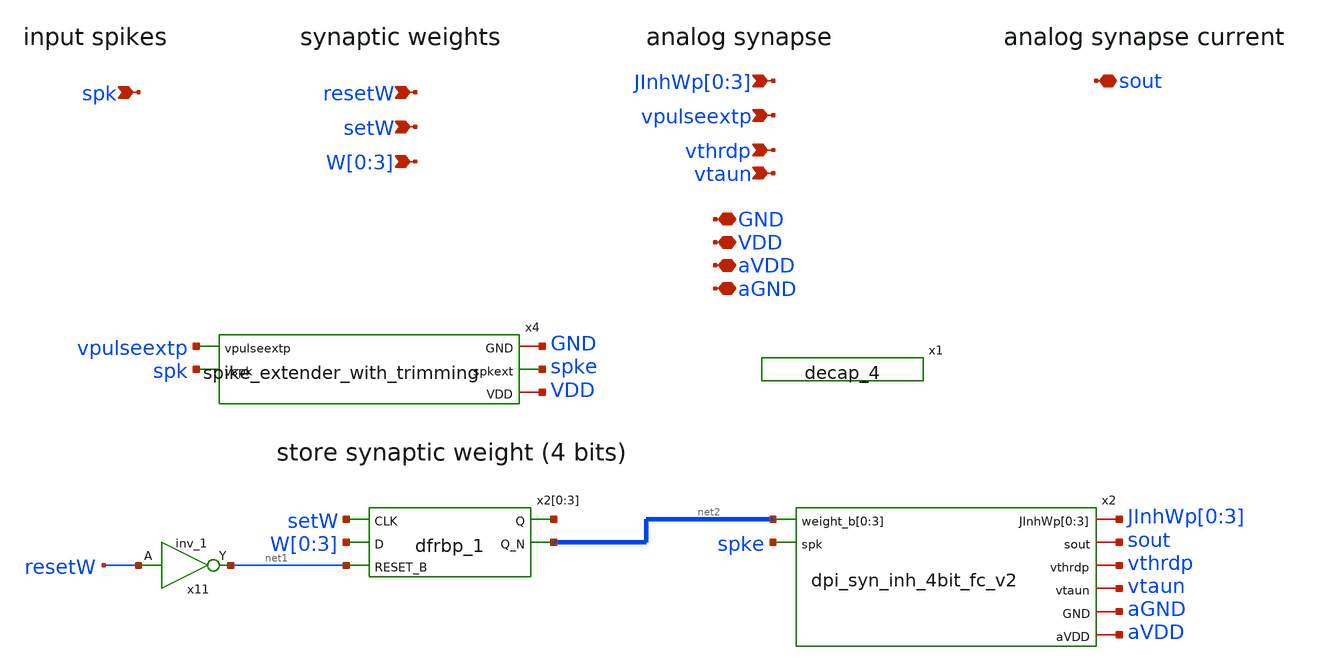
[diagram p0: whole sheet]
** sch_path: design/xschem/synapse_4bit_memory_inh_v1_norail.sch
**.subckt synapse_4bit_memory_inh_v1_norail vpulseextp spk JInhWp[0],JInhWp[1],JInhWp[2],JInhWp[3]
*+ W[0],W[1],W[2],W[3] setW resetW sout vthrdp vtaun GND VDD aVDD aGND
*.ipin vpulseextp
*.ipin spk
*.ipin JInhWp[0],JInhWp[1],JInhWp[2],JInhWp[3]
*.ipin W[0],W[1],W[2],W[3]
*.ipin setW
*.ipin resetW
*.iopin sout
*.ipin vthrdp
*.ipin vtaun
*.iopin GND
*.iopin VDD
*.iopin aVDD
*.iopin aGND
x11 resetW GND GND VDD VDD net1 sky130_fd_sc_hd__inv_1
x2 JInhWp[0] JInhWp[1] JInhWp[2] JInhWp[3] net2[3] net2[2] net2[1] net2[0] spke sout vthrdp vtaun
+ aGND aVDD dpi_syn_inh_4bit_fc_v2
x2[0] setW W[0] net1 GND GND VDD VDD net3[3] net2[3] sky130_fd_sc_hd__dfrbp_1
x2[1] setW W[1] net1 GND GND VDD VDD net3[2] net2[2] sky130_fd_sc_hd__dfrbp_1
x2[2] setW W[2] net1 GND GND VDD VDD net3[1] net2[1] sky130_fd_sc_hd__dfrbp_1
x2[3] setW W[3] net1 GND GND VDD VDD net3[0] net2[0] sky130_fd_sc_hd__dfrbp_1
x4 vpulseextp spk GND spke VDD spike_extender_with_trimming
x1 GND GND VDD VDD sky130_fd_sc_hd__decap_4
**.ends

* expanding   symbol:  dpi_syn_inh_4bit_fc_v2.sym # of pins=8
** sym_path: design/xschem/dpi_syn_inh_4bit_fc_v2.sym
** sch_path: design/xschem/dpi_syn_inh_4bit_fc_v2.sch
.subckt dpi_syn_inh_4bit_fc_v2 JInhWp[0] JInhWp[1] JInhWp[2] JInhWp[3] weight_b[0] weight_b[1]
+ weight_b[2] weight_b[3] spk sout vthrdp vtaun GND aVDD
*.ipin spk
*.iopin vthrdp
*.iopin vtaun
*.iopin sout
*.iopin GND
*.iopin aVDD
*.ipin weight_b[0],weight_b[1],weight_b[2],weight_b[3]
*.iopin JInhWp[0],JInhWp[1],JInhWp[2],JInhWp[3]
XM5 net2 net3 net1 aVDD sky130_fd_pr__pfet_01v8 L=0.2 W=1.2 nf=1 ad='int((nf+1)/2) * W/nf * 0.29' as='int((nf+2)/2) * W/nf * 0.29'
+ pd='2*int((nf+1)/2) * (W/nf + 0.29)' ps='2*int((nf+2)/2) * (W/nf + 0.29)' nrd='0.29 / W' nrs='0.29 / W'
+ sa=0 sb=0 sd=0 mult=1 m=1
XM2 GND vthrdp net2 aVDD sky130_fd_pr__pfet_01v8 L=0.2 W=1.2 nf=1 ad='int((nf+1)/2) * W/nf * 0.29' as='int((nf+2)/2) * W/nf * 0.29'
+ pd='2*int((nf+1)/2) * (W/nf + 0.29)' ps='2*int((nf+2)/2) * (W/nf + 0.29)' nrd='0.29 / W' nrs='0.29 / W'
+ sa=0 sb=0 sd=0 mult=1 m=1
XM3 vsin vsin net2 aVDD sky130_fd_pr__pfet_01v8 L=0.2 W=1.2 nf=1 ad='int((nf+1)/2) * W/nf * 0.29' as='int((nf+2)/2) * W/nf * 0.29'
+ pd='2*int((nf+1)/2) * (W/nf + 0.29)' ps='2*int((nf+2)/2) * (W/nf + 0.29)' nrd='0.29 / W' nrs='0.29 / W'
+ sa=0 sb=0 sd=0 mult=1 m=1
XM4 vsin vtaun GND GND sky130_fd_pr__nfet_01v8 L=0.25 W=1.0 nf=1 ad='int((nf+1)/2) * W/nf * 0.29' as='int((nf+2)/2) * W/nf * 0.29'
+ pd='2*int((nf+1)/2) * (W/nf + 0.29)' ps='2*int((nf+2)/2) * (W/nf + 0.29)' nrd='0.29 / W' nrs='0.29 / W'
+ sa=0 sb=0 sd=0 mult=1 m=1
XM6 sout vsin GND GND sky130_fd_pr__nfet_01v8 L=0.25 W=1.0 nf=1 ad='int((nf+1)/2) * W/nf * 0.29' as='int((nf+2)/2) * W/nf * 0.29'
+ pd='2*int((nf+1)/2) * (W/nf + 0.29)' ps='2*int((nf+2)/2) * (W/nf + 0.29)' nrd='0.29 / W' nrs='0.29 / W'
+ sa=0 sb=0 sd=0 mult=1 m=1
XM7 net3 spk GND GND sky130_fd_pr__nfet_01v8 L=0.25 W=1.0 nf=1 ad='int((nf+1)/2) * W/nf * 0.29' as='int((nf+2)/2) * W/nf * 0.29'
+ pd='2*int((nf+1)/2) * (W/nf + 0.29)' ps='2*int((nf+2)/2) * (W/nf + 0.29)' nrd='0.29 / W' nrs='0.29 / W'
+ sa=0 sb=0 sd=0 mult=1 m=1
XM8 net3 spk aVDD aVDD sky130_fd_pr__pfet_01v8 L=0.2 W=1.2 nf=1 ad='int((nf+1)/2) * W/nf * 0.29' as='int((nf+2)/2) * W/nf * 0.29'
+ pd='2*int((nf+1)/2) * (W/nf + 0.29)' ps='2*int((nf+2)/2) * (W/nf + 0.29)' nrd='0.29 / W' nrs='0.29 / W'
+ sa=0 sb=0 sd=0 mult=1 m=1
XC1 vsin GND sky130_fd_pr__cap_mim_m3_1 W=5 L=5 MF=1 m=1
XM9 net4 JInhWp[0] aVDD aVDD sky130_fd_pr__pfet_01v8 L=1.2 W=1.2 nf=1 ad='int((nf+1)/2) * W/nf * 0.29'
+ as='int((nf+2)/2) * W/nf * 0.29' pd='2*int((nf+1)/2) * (W/nf + 0.29)' ps='2*int((nf+2)/2) * (W/nf + 0.29)'
+ nrd='0.29 / W' nrs='0.29 / W' sa=0 sb=0 sd=0 mult=1 m=1
XM10 net1 weight_b[0] net4 aVDD sky130_fd_pr__pfet_01v8 L=0.2 W=1.2 nf=1 ad='int((nf+1)/2) * W/nf * 0.29'
+ as='int((nf+2)/2) * W/nf * 0.29' pd='2*int((nf+1)/2) * (W/nf + 0.29)' ps='2*int((nf+2)/2) * (W/nf + 0.29)'
+ nrd='0.29 / W' nrs='0.29 / W' sa=0 sb=0 sd=0 mult=1 m=1
XM11 net1 weight_b[1] net5 aVDD sky130_fd_pr__pfet_01v8 L=0.2 W=1.2 nf=1 ad='int((nf+1)/2) * W/nf * 0.29'
+ as='int((nf+2)/2) * W/nf * 0.29' pd='2*int((nf+1)/2) * (W/nf + 0.29)' ps='2*int((nf+2)/2) * (W/nf + 0.29)'
+ nrd='0.29 / W' nrs='0.29 / W' sa=0 sb=0 sd=0 mult=1 m=1
XM1 net5 JInhWp[1] aVDD aVDD sky130_fd_pr__pfet_01v8 L=2.0 W=1.2 nf=1 ad='int((nf+1)/2) * W/nf * 0.29'
+ as='int((nf+2)/2) * W/nf * 0.29' pd='2*int((nf+1)/2) * (W/nf + 0.29)' ps='2*int((nf+2)/2) * (W/nf + 0.29)'
+ nrd='0.29 / W' nrs='0.29 / W' sa=0 sb=0 sd=0 mult=1 m=1
XM12 net6 JInhWp[2] aVDD aVDD sky130_fd_pr__pfet_01v8 L=4.0 W=1.2 nf=1 ad='int((nf+1)/2) * W/nf * 0.29'
+ as='int((nf+2)/2) * W/nf * 0.29' pd='2*int((nf+1)/2) * (W/nf + 0.29)' ps='2*int((nf+2)/2) * (W/nf + 0.29)'
+ nrd='0.29 / W' nrs='0.29 / W' sa=0 sb=0 sd=0 mult=1 m=1
XM13 net7 JInhWp[3] aVDD aVDD sky130_fd_pr__pfet_01v8 L=8.0 W=1.2 nf=1 ad='int((nf+1)/2) * W/nf * 0.29'
+ as='int((nf+2)/2) * W/nf * 0.29' pd='2*int((nf+1)/2) * (W/nf + 0.29)' ps='2*int((nf+2)/2) * (W/nf + 0.29)'
+ nrd='0.29 / W' nrs='0.29 / W' sa=0 sb=0 sd=0 mult=1 m=1
XM14 net1 weight_b[2] net6 aVDD sky130_fd_pr__pfet_01v8 L=0.2 W=1.2 nf=1 ad='int((nf+1)/2) * W/nf * 0.29'
+ as='int((nf+2)/2) * W/nf * 0.29' pd='2*int((nf+1)/2) * (W/nf + 0.29)' ps='2*int((nf+2)/2) * (W/nf + 0.29)'
+ nrd='0.29 / W' nrs='0.29 / W' sa=0 sb=0 sd=0 mult=1 m=1
XM15 net1 weight_b[3] net7 aVDD sky130_fd_pr__pfet_01v8 L=0.2 W=1.2 nf=1 ad='int((nf+1)/2) * W/nf * 0.29'
+ as='int((nf+2)/2) * W/nf * 0.29' pd='2*int((nf+1)/2) * (W/nf + 0.29)' ps='2*int((nf+2)/2) * (W/nf + 0.29)'
+ nrd='0.29 / W' nrs='0.29 / W' sa=0 sb=0 sd=0 mult=1 m=1
.ends


* expanding   symbol:  spike_extender_with_trimming.sym # of pins=5
** sym_path: design/xschem/spike_extender_with_trimming.sym
** sch_path: design/xschem/spike_extender_with_trimming.sch
.subckt spike_extender_with_trimming vpulseextp vspk GND spkext VDD
*.iopin GND
*.iopin VDD
*.ipin vspk
*.opin spkext
*.ipin vpulseextp
x1 vpulseextp vpulseshort GND spkext VDD spike_extender
x3 vspk GND GND VDD VDD net1 sky130_fd_sc_hd__clkdlybuf4s50_1
x2 net1 vspk GND GND VDD VDD vpulseshort sky130_fd_sc_hd__nor2b_1
.ends


* expanding   symbol:  spike_extender.sym # of pins=5
** sym_path: design/xschem/spike_extender.sym
** sch_path: design/xschem/spike_extender.sch
.subckt spike_extender vpulseextp spk GND spkext VDD
*.iopin GND
*.iopin VDD
*.ipin spk
*.opin spkext
*.ipin vpulseextp
XM1 net1 spk GND GND sky130_fd_pr__nfet_01v8 L=0.15 W=0.65 nf=1 ad='int((nf+1)/2) * W/nf * 0.29' as='int((nf+2)/2) * W/nf * 0.29'
+ pd='2*int((nf+1)/2) * (W/nf + 0.29)' ps='2*int((nf+2)/2) * (W/nf + 0.29)' nrd='0.29 / W' nrs='0.29 / W'
+ sa=0 sb=0 sd=0 mult=1 m=1
XM6 net1 vpulseextp VDD VDD sky130_fd_pr__pfet_01v8 L=2 W=1 nf=1 ad='int((nf+1)/2) * W/nf * 0.29' as='int((nf+2)/2) * W/nf * 0.29'
+ pd='2*int((nf+1)/2) * (W/nf + 0.29)' ps='2*int((nf+2)/2) * (W/nf + 0.29)' nrd='0.29 / W' nrs='0.29 / W'
+ sa=0 sb=0 sd=0 mult=1 m=1
XM5 net3 net2 GND GND sky130_fd_pr__nfet_01v8 L=0.15 W=0.65 nf=1 ad='int((nf+1)/2) * W/nf * 0.29' as='int((nf+2)/2) * W/nf * 0.29'
+ pd='2*int((nf+1)/2) * (W/nf + 0.29)' ps='2*int((nf+2)/2) * (W/nf + 0.29)' nrd='0.29 / W' nrs='0.29 / W'
+ sa=0 sb=0 sd=0 mult=1 m=1
XM8 spkext net3 GND GND sky130_fd_pr__nfet_01v8 L=0.15 W=0.65 nf=1 ad='int((nf+1)/2) * W/nf * 0.29' as='int((nf+2)/2) * W/nf * 0.29'
+ pd='2*int((nf+1)/2) * (W/nf + 0.29)' ps='2*int((nf+2)/2) * (W/nf + 0.29)' nrd='0.29 / W' nrs='0.29 / W'
+ sa=0 sb=0 sd=0 mult=1 m=1
XM4 net3 net2 VDD VDD sky130_fd_pr__pfet_01v8 L=0.15 W=1.0 nf=1 ad='int((nf+1)/2) * W/nf * 0.29' as='int((nf+2)/2) * W/nf * 0.29'
+ pd='2*int((nf+1)/2) * (W/nf + 0.29)' ps='2*int((nf+2)/2) * (W/nf + 0.29)' nrd='0.29 / W' nrs='0.29 / W'
+ sa=0 sb=0 sd=0 mult=1 m=1
XM7 spkext net3 VDD VDD sky130_fd_pr__pfet_01v8 L=0.15 W=1.0 nf=1 ad='int((nf+1)/2) * W/nf * 0.29' as='int((nf+2)/2) * W/nf * 0.29'
+ pd='2*int((nf+1)/2) * (W/nf + 0.29)' ps='2*int((nf+2)/2) * (W/nf + 0.29)' nrd='0.29 / W' nrs='0.29 / W'
+ sa=0 sb=0 sd=0 mult=1 m=1
XM2 net2 net1 GND GND sky130_fd_pr__nfet_01v8 L=0.15 W=0.65 nf=1 ad='int((nf+1)/2) * W/nf * 0.29' as='int((nf+2)/2) * W/nf * 0.29'
+ pd='2*int((nf+1)/2) * (W/nf + 0.29)' ps='2*int((nf+2)/2) * (W/nf + 0.29)' nrd='0.29 / W' nrs='0.29 / W'
+ sa=0 sb=0 sd=0 mult=1 m=1
XM3 net2 net1 VDD VDD sky130_fd_pr__pfet_01v8 L=0.15 W=1.0 nf=1 ad='int((nf+1)/2) * W/nf * 0.29' as='int((nf+2)/2) * W/nf * 0.29'
+ pd='2*int((nf+1)/2) * (W/nf + 0.29)' ps='2*int((nf+2)/2) * (W/nf + 0.29)' nrd='0.29 / W' nrs='0.29 / W'
+ sa=0 sb=0 sd=0 mult=1 m=1
XM9 GND net1 GND GND sky130_fd_pr__nfet_01v8 L=1 W=0.65 nf=1 ad='int((nf+1)/2) * W/nf * 0.29' as='int((nf+2)/2) * W/nf * 0.29'
+ pd='2*int((nf+1)/2) * (W/nf + 0.29)' ps='2*int((nf+2)/2) * (W/nf + 0.29)' nrd='0.29 / W' nrs='0.29 / W'
+ sa=0 sb=0 sd=0 mult=1 m=1
.ends

.end
